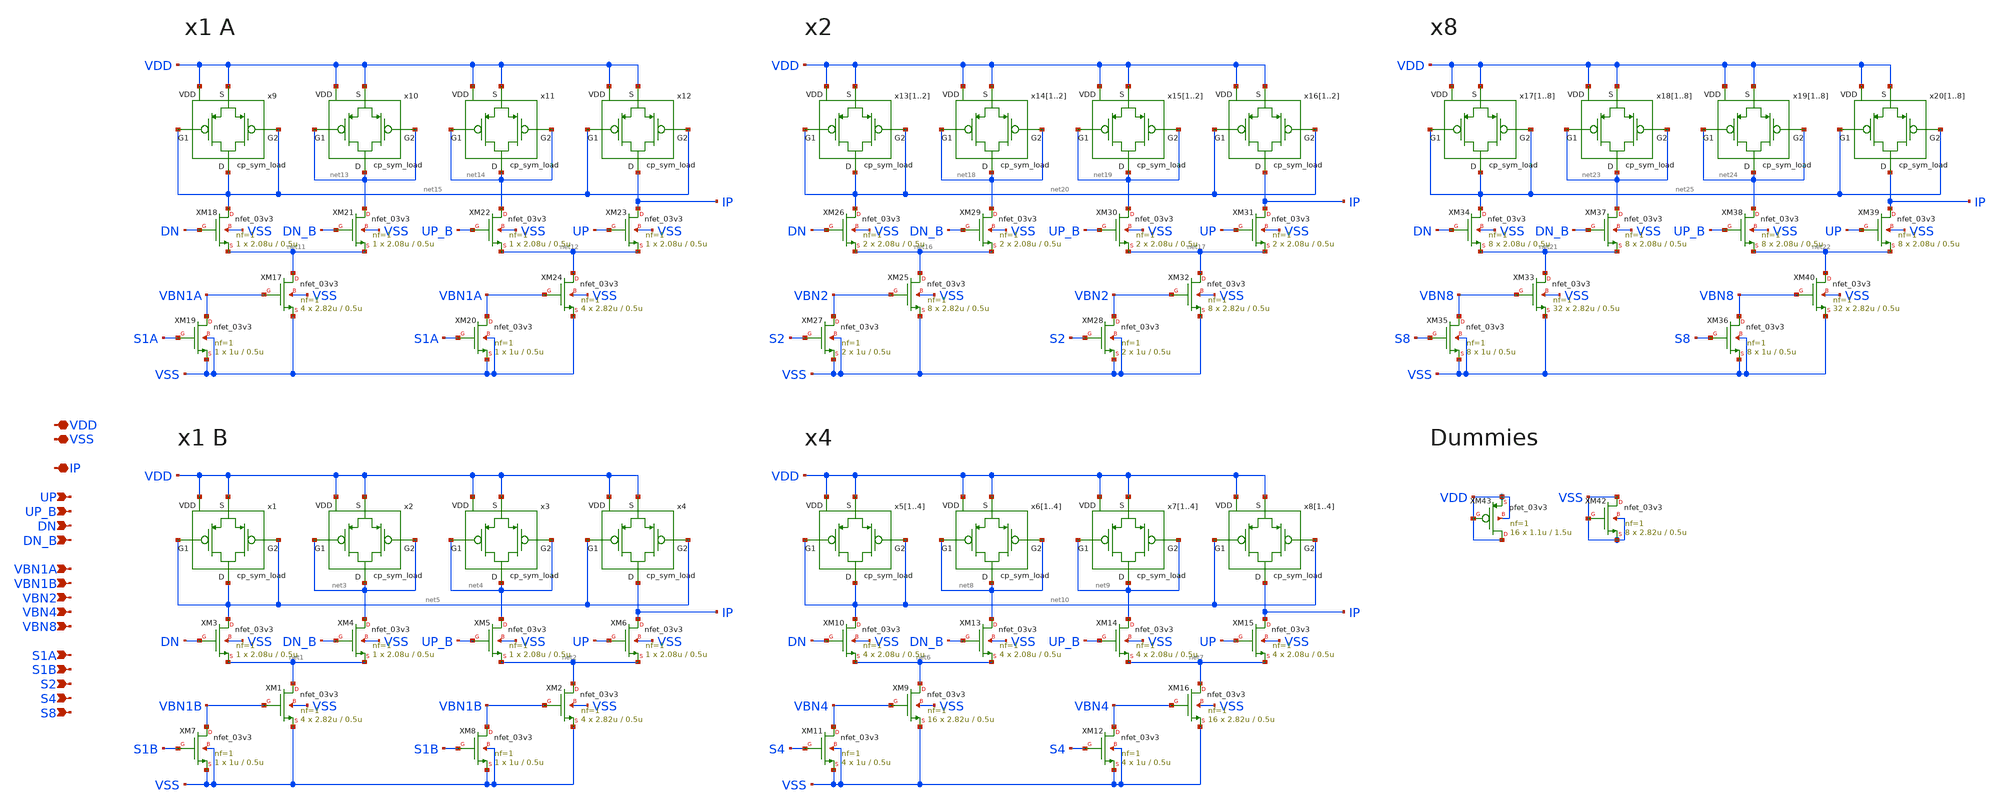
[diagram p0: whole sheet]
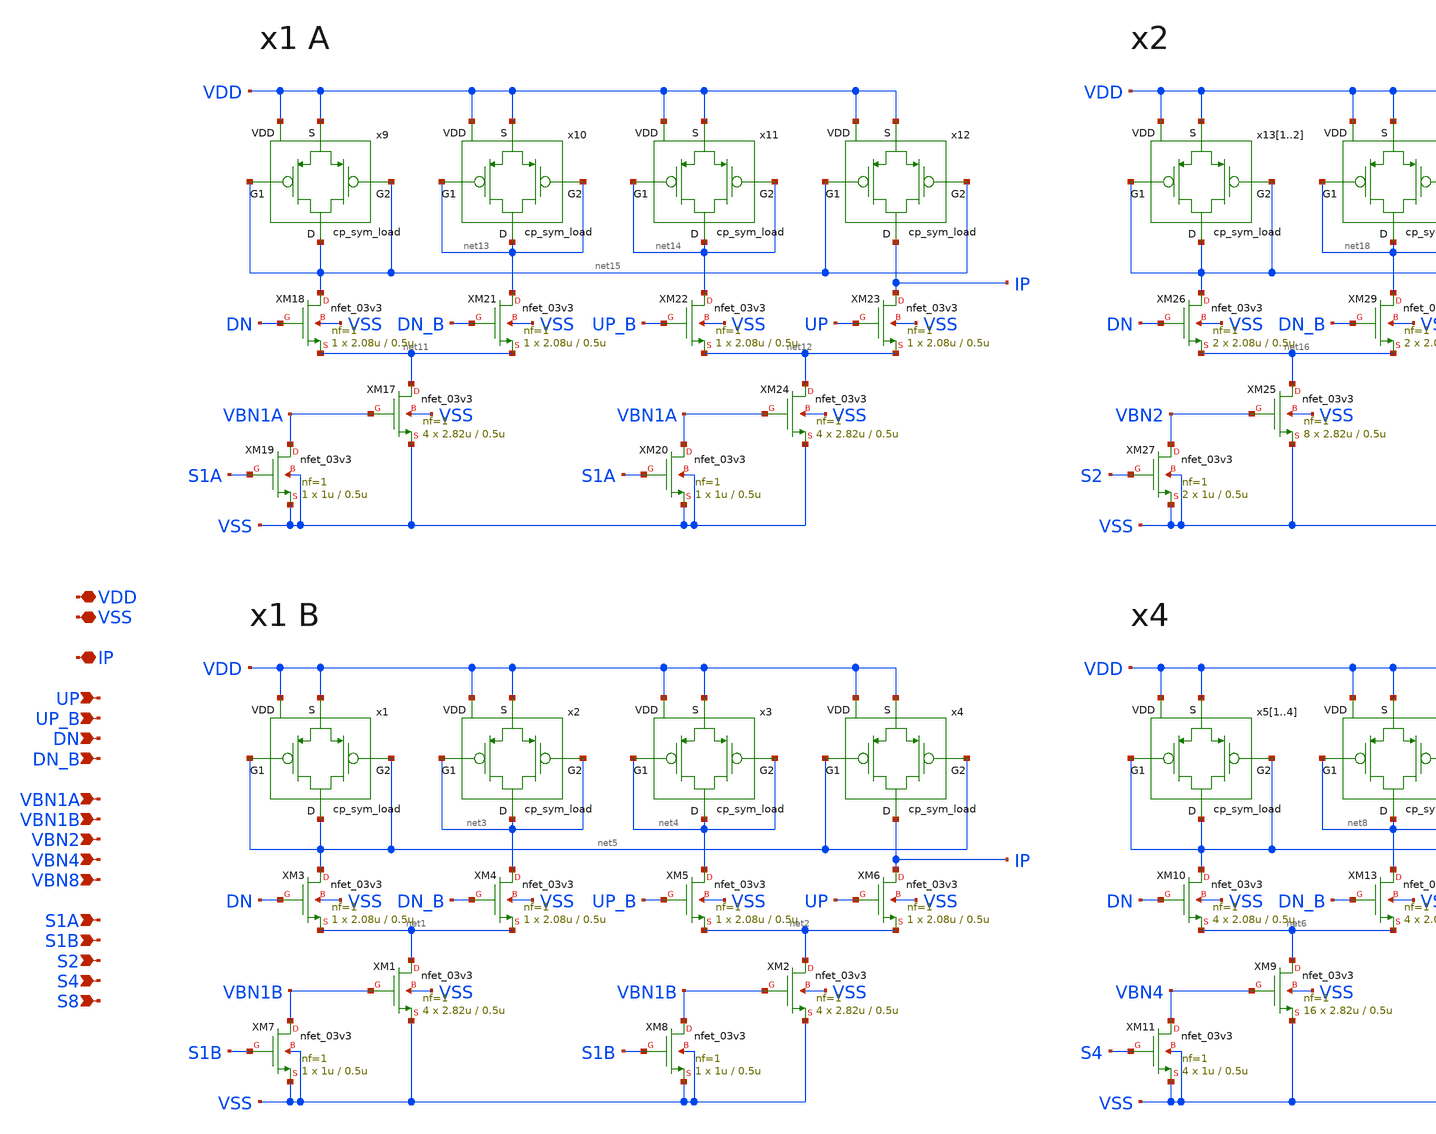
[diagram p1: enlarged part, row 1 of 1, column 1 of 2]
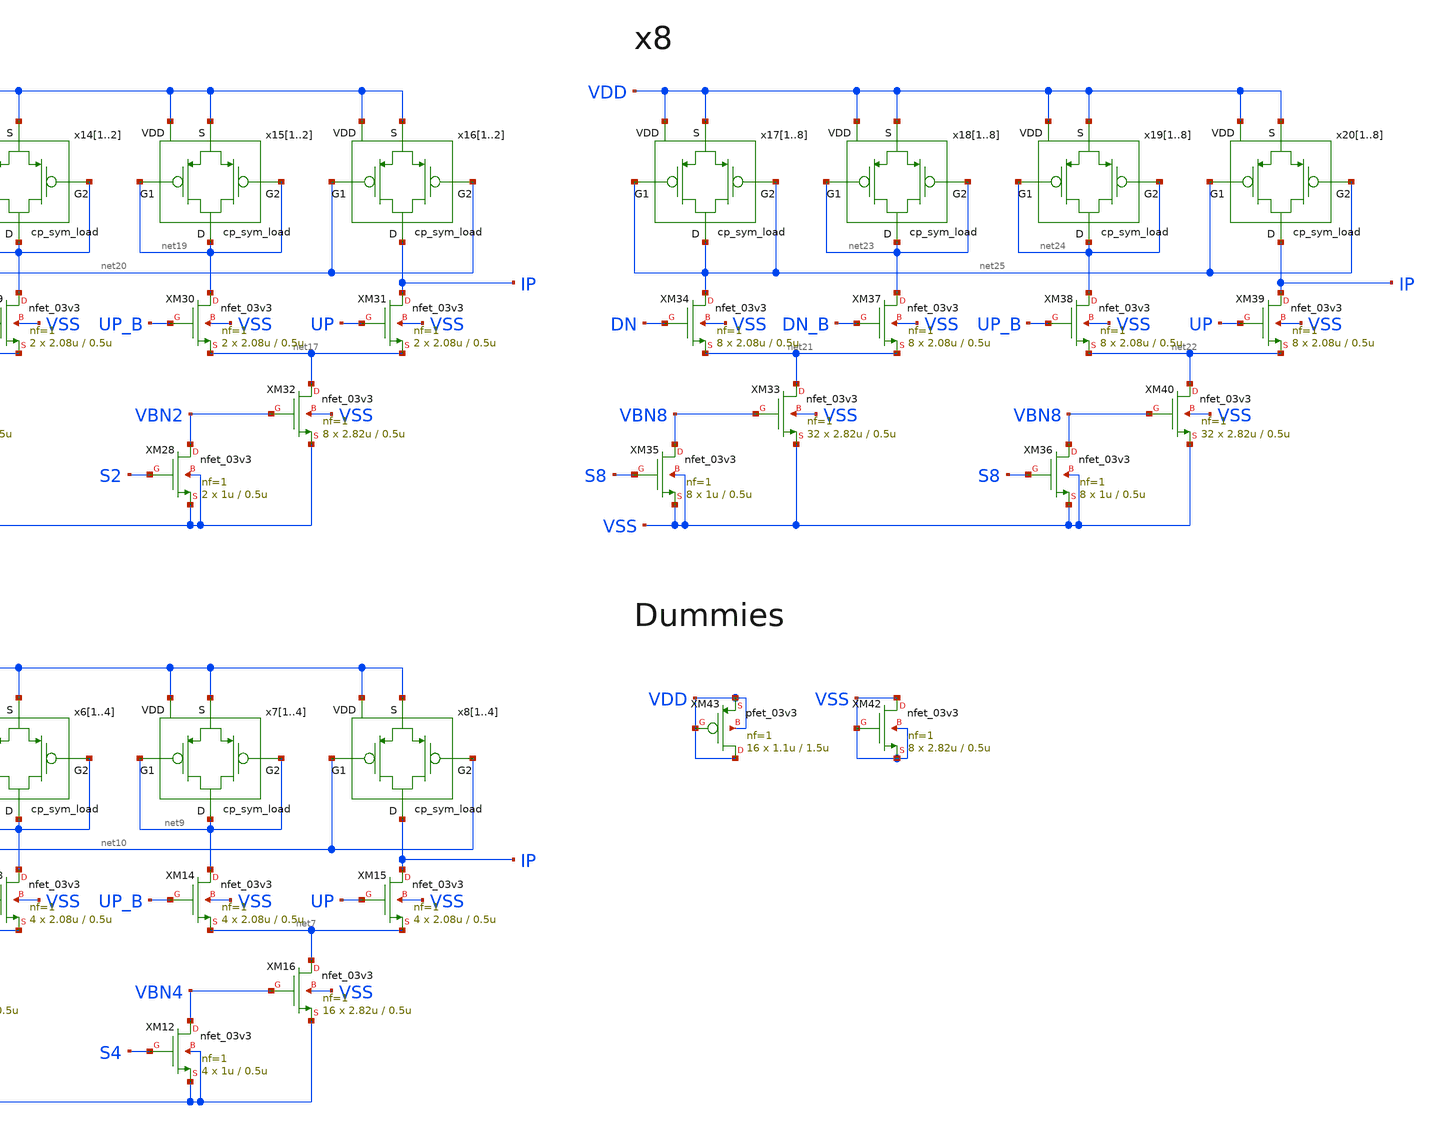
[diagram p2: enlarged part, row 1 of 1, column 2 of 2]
** sch_path: designs/libs/core_analog/charge_pump/charge_pump_top.sch
**.subckt charge_pump_top VDD VSS UP UP_B DN DN_B VBN1A IP S1A VBN1B VBN2 VBN4 VBN8 S1B S2 S4 S8
*.iopin VDD
*.iopin VSS
*.ipin UP
*.ipin UP_B
*.ipin DN
*.ipin DN_B
*.ipin VBN1A
*.iopin IP
*.ipin S1A
*.ipin VBN1B
*.ipin VBN2
*.ipin VBN4
*.ipin VBN8
*.ipin S1B
*.ipin S2
*.ipin S4
*.ipin S8
x1 net5 net5 VDD net5 VDD cp_sym_load
x2 net3 net3 VDD net3 VDD cp_sym_load
x3 net4 net4 VDD net4 VDD cp_sym_load
x4 net5 net5 VDD IP VDD cp_sym_load
XM1 net1 VBN1B VSS VSS nfet_03v3 L=0.5u W=2.82u nf=1 ad='int((nf+1)/2) * W/nf * 0.18u' as='int((nf+2)/2) * W/nf * 0.18u'
+ pd='2*int((nf+1)/2) * (W/nf + 0.18u)' ps='2*int((nf+2)/2) * (W/nf + 0.18u)' nrd='0.18u / W' nrs='0.18u / W'
+ sa=0 sb=0 sd=0 m=4
XM3 net5 DN net1 VSS nfet_03v3 L=0.5u W=2.08u nf=1 ad='int((nf+1)/2) * W/nf * 0.18u' as='int((nf+2)/2) * W/nf * 0.18u'
+ pd='2*int((nf+1)/2) * (W/nf + 0.18u)' ps='2*int((nf+2)/2) * (W/nf + 0.18u)' nrd='0.18u / W' nrs='0.18u / W'
+ sa=0 sb=0 sd=0 m=1
XM7 VBN1B S1B VSS VSS nfet_03v3 L=0.5u W=1u nf=1 ad='int((nf+1)/2) * W/nf * 0.18u' as='int((nf+2)/2) * W/nf * 0.18u'
+ pd='2*int((nf+1)/2) * (W/nf + 0.18u)' ps='2*int((nf+2)/2) * (W/nf + 0.18u)' nrd='0.18u / W' nrs='0.18u / W'
+ sa=0 sb=0 sd=0 m=1
XM8 VBN1B S1B VSS VSS nfet_03v3 L=0.5u W=1u nf=1 ad='int((nf+1)/2) * W/nf * 0.18u' as='int((nf+2)/2) * W/nf * 0.18u'
+ pd='2*int((nf+1)/2) * (W/nf + 0.18u)' ps='2*int((nf+2)/2) * (W/nf + 0.18u)' nrd='0.18u / W' nrs='0.18u / W'
+ sa=0 sb=0 sd=0 m=1
XM4 net3 DN_B net1 VSS nfet_03v3 L=0.5u W=2.08u nf=1 ad='int((nf+1)/2) * W/nf * 0.18u' as='int((nf+2)/2) * W/nf * 0.18u'
+ pd='2*int((nf+1)/2) * (W/nf + 0.18u)' ps='2*int((nf+2)/2) * (W/nf + 0.18u)' nrd='0.18u / W' nrs='0.18u / W'
+ sa=0 sb=0 sd=0 m=1
XM5 net4 UP_B net2 VSS nfet_03v3 L=0.5u W=2.08u nf=1 ad='int((nf+1)/2) * W/nf * 0.18u' as='int((nf+2)/2) * W/nf * 0.18u'
+ pd='2*int((nf+1)/2) * (W/nf + 0.18u)' ps='2*int((nf+2)/2) * (W/nf + 0.18u)' nrd='0.18u / W' nrs='0.18u / W'
+ sa=0 sb=0 sd=0 m=1
XM6 IP UP net2 VSS nfet_03v3 L=0.5u W=2.08u nf=1 ad='int((nf+1)/2) * W/nf * 0.18u' as='int((nf+2)/2) * W/nf * 0.18u'
+ pd='2*int((nf+1)/2) * (W/nf + 0.18u)' ps='2*int((nf+2)/2) * (W/nf + 0.18u)' nrd='0.18u / W' nrs='0.18u / W'
+ sa=0 sb=0 sd=0 m=1
XM2 net2 VBN1B VSS VSS nfet_03v3 L=0.5u W=2.82u nf=1 ad='int((nf+1)/2) * W/nf * 0.18u' as='int((nf+2)/2) * W/nf * 0.18u'
+ pd='2*int((nf+1)/2) * (W/nf + 0.18u)' ps='2*int((nf+2)/2) * (W/nf + 0.18u)' nrd='0.18u / W' nrs='0.18u / W'
+ sa=0 sb=0 sd=0 m=4
x51 net10 net10 VDD net10 VDD cp_sym_load
x52 net10 net10 VDD net10 VDD cp_sym_load
x53 net10 net10 VDD net10 VDD cp_sym_load
x54 net10 net10 VDD net10 VDD cp_sym_load
x61 net8 net8 VDD net8 VDD cp_sym_load
x62 net8 net8 VDD net8 VDD cp_sym_load
x63 net8 net8 VDD net8 VDD cp_sym_load
x64 net8 net8 VDD net8 VDD cp_sym_load
x71 net9 net9 VDD net9 VDD cp_sym_load
x72 net9 net9 VDD net9 VDD cp_sym_load
x73 net9 net9 VDD net9 VDD cp_sym_load
x74 net9 net9 VDD net9 VDD cp_sym_load
x81 net10 net10 VDD IP VDD cp_sym_load
x82 net10 net10 VDD IP VDD cp_sym_load
x83 net10 net10 VDD IP VDD cp_sym_load
x84 net10 net10 VDD IP VDD cp_sym_load
XM9 net6 VBN4 VSS VSS nfet_03v3 L=0.5u W=2.82u nf=1 ad='int((nf+1)/2) * W/nf * 0.18u' as='int((nf+2)/2) * W/nf * 0.18u'
+ pd='2*int((nf+1)/2) * (W/nf + 0.18u)' ps='2*int((nf+2)/2) * (W/nf + 0.18u)' nrd='0.18u / W' nrs='0.18u / W'
+ sa=0 sb=0 sd=0 m=16
XM10 net10 DN net6 VSS nfet_03v3 L=0.5u W=2.08u nf=1 ad='int((nf+1)/2) * W/nf * 0.18u' as='int((nf+2)/2) * W/nf * 0.18u'
+ pd='2*int((nf+1)/2) * (W/nf + 0.18u)' ps='2*int((nf+2)/2) * (W/nf + 0.18u)' nrd='0.18u / W' nrs='0.18u / W'
+ sa=0 sb=0 sd=0 m=4
XM11 VBN4 S4 VSS VSS nfet_03v3 L=0.5u W=1u nf=1 ad='int((nf+1)/2) * W/nf * 0.18u' as='int((nf+2)/2) * W/nf * 0.18u'
+ pd='2*int((nf+1)/2) * (W/nf + 0.18u)' ps='2*int((nf+2)/2) * (W/nf + 0.18u)' nrd='0.18u / W' nrs='0.18u / W'
+ sa=0 sb=0 sd=0 m=4
XM12 VBN4 S4 VSS VSS nfet_03v3 L=0.5u W=1u nf=1 ad='int((nf+1)/2) * W/nf * 0.18u' as='int((nf+2)/2) * W/nf * 0.18u'
+ pd='2*int((nf+1)/2) * (W/nf + 0.18u)' ps='2*int((nf+2)/2) * (W/nf + 0.18u)' nrd='0.18u / W' nrs='0.18u / W'
+ sa=0 sb=0 sd=0 m=4
XM13 net8 DN_B net6 VSS nfet_03v3 L=0.5u W=2.08u nf=1 ad='int((nf+1)/2) * W/nf * 0.18u' as='int((nf+2)/2) * W/nf * 0.18u'
+ pd='2*int((nf+1)/2) * (W/nf + 0.18u)' ps='2*int((nf+2)/2) * (W/nf + 0.18u)' nrd='0.18u / W' nrs='0.18u / W'
+ sa=0 sb=0 sd=0 m=4
XM14 net9 UP_B net7 VSS nfet_03v3 L=0.5u W=2.08u nf=1 ad='int((nf+1)/2) * W/nf * 0.18u' as='int((nf+2)/2) * W/nf * 0.18u'
+ pd='2*int((nf+1)/2) * (W/nf + 0.18u)' ps='2*int((nf+2)/2) * (W/nf + 0.18u)' nrd='0.18u / W' nrs='0.18u / W'
+ sa=0 sb=0 sd=0 m=4
XM15 IP UP net7 VSS nfet_03v3 L=0.5u W=2.08u nf=1 ad='int((nf+1)/2) * W/nf * 0.18u' as='int((nf+2)/2) * W/nf * 0.18u'
+ pd='2*int((nf+1)/2) * (W/nf + 0.18u)' ps='2*int((nf+2)/2) * (W/nf + 0.18u)' nrd='0.18u / W' nrs='0.18u / W'
+ sa=0 sb=0 sd=0 m=4
XM16 net7 VBN4 VSS VSS nfet_03v3 L=0.5u W=2.82u nf=1 ad='int((nf+1)/2) * W/nf * 0.18u' as='int((nf+2)/2) * W/nf * 0.18u'
+ pd='2*int((nf+1)/2) * (W/nf + 0.18u)' ps='2*int((nf+2)/2) * (W/nf + 0.18u)' nrd='0.18u / W' nrs='0.18u / W'
+ sa=0 sb=0 sd=0 m=16
x9 net15 net15 VDD net15 VDD cp_sym_load
x10 net13 net13 VDD net13 VDD cp_sym_load
x11 net14 net14 VDD net14 VDD cp_sym_load
x12 net15 net15 VDD IP VDD cp_sym_load
XM17 net11 VBN1A VSS VSS nfet_03v3 L=0.5u W=2.82u nf=1 ad='int((nf+1)/2) * W/nf * 0.18u' as='int((nf+2)/2) * W/nf * 0.18u'
+ pd='2*int((nf+1)/2) * (W/nf + 0.18u)' ps='2*int((nf+2)/2) * (W/nf + 0.18u)' nrd='0.18u / W' nrs='0.18u / W'
+ sa=0 sb=0 sd=0 m=4
XM18 net15 DN net11 VSS nfet_03v3 L=0.5u W=2.08u nf=1 ad='int((nf+1)/2) * W/nf * 0.18u' as='int((nf+2)/2) * W/nf * 0.18u'
+ pd='2*int((nf+1)/2) * (W/nf + 0.18u)' ps='2*int((nf+2)/2) * (W/nf + 0.18u)' nrd='0.18u / W' nrs='0.18u / W'
+ sa=0 sb=0 sd=0 m=1
XM19 VBN1A S1A VSS VSS nfet_03v3 L=0.5u W=1u nf=1 ad='int((nf+1)/2) * W/nf * 0.18u' as='int((nf+2)/2) * W/nf * 0.18u'
+ pd='2*int((nf+1)/2) * (W/nf + 0.18u)' ps='2*int((nf+2)/2) * (W/nf + 0.18u)' nrd='0.18u / W' nrs='0.18u / W'
+ sa=0 sb=0 sd=0 m=1
XM20 VBN1A S1A VSS VSS nfet_03v3 L=0.5u W=1u nf=1 ad='int((nf+1)/2) * W/nf * 0.18u' as='int((nf+2)/2) * W/nf * 0.18u'
+ pd='2*int((nf+1)/2) * (W/nf + 0.18u)' ps='2*int((nf+2)/2) * (W/nf + 0.18u)' nrd='0.18u / W' nrs='0.18u / W'
+ sa=0 sb=0 sd=0 m=1
XM21 net13 DN_B net11 VSS nfet_03v3 L=0.5u W=2.08u nf=1 ad='int((nf+1)/2) * W/nf * 0.18u' as='int((nf+2)/2) * W/nf * 0.18u'
+ pd='2*int((nf+1)/2) * (W/nf + 0.18u)' ps='2*int((nf+2)/2) * (W/nf + 0.18u)' nrd='0.18u / W' nrs='0.18u / W'
+ sa=0 sb=0 sd=0 m=1
XM22 net14 UP_B net12 VSS nfet_03v3 L=0.5u W=2.08u nf=1 ad='int((nf+1)/2) * W/nf * 0.18u' as='int((nf+2)/2) * W/nf * 0.18u'
+ pd='2*int((nf+1)/2) * (W/nf + 0.18u)' ps='2*int((nf+2)/2) * (W/nf + 0.18u)' nrd='0.18u / W' nrs='0.18u / W'
+ sa=0 sb=0 sd=0 m=1
XM23 IP UP net12 VSS nfet_03v3 L=0.5u W=2.08u nf=1 ad='int((nf+1)/2) * W/nf * 0.18u' as='int((nf+2)/2) * W/nf * 0.18u'
+ pd='2*int((nf+1)/2) * (W/nf + 0.18u)' ps='2*int((nf+2)/2) * (W/nf + 0.18u)' nrd='0.18u / W' nrs='0.18u / W'
+ sa=0 sb=0 sd=0 m=1
XM24 net12 VBN1A VSS VSS nfet_03v3 L=0.5u W=2.82u nf=1 ad='int((nf+1)/2) * W/nf * 0.18u' as='int((nf+2)/2) * W/nf * 0.18u'
+ pd='2*int((nf+1)/2) * (W/nf + 0.18u)' ps='2*int((nf+2)/2) * (W/nf + 0.18u)' nrd='0.18u / W' nrs='0.18u / W'
+ sa=0 sb=0 sd=0 m=4
x131 net20 net20 VDD net20 VDD cp_sym_load
x132 net20 net20 VDD net20 VDD cp_sym_load
x141 net18 net18 VDD net18 VDD cp_sym_load
x142 net18 net18 VDD net18 VDD cp_sym_load
x151 net19 net19 VDD net19 VDD cp_sym_load
x152 net19 net19 VDD net19 VDD cp_sym_load
x161 net20 net20 VDD IP VDD cp_sym_load
x162 net20 net20 VDD IP VDD cp_sym_load
XM25 net16 VBN2 VSS VSS nfet_03v3 L=0.5u W=2.82u nf=1 ad='int((nf+1)/2) * W/nf * 0.18u' as='int((nf+2)/2) * W/nf * 0.18u'
+ pd='2*int((nf+1)/2) * (W/nf + 0.18u)' ps='2*int((nf+2)/2) * (W/nf + 0.18u)' nrd='0.18u / W' nrs='0.18u / W'
+ sa=0 sb=0 sd=0 m=8
XM26 net20 DN net16 VSS nfet_03v3 L=0.5u W=2.08u nf=1 ad='int((nf+1)/2) * W/nf * 0.18u' as='int((nf+2)/2) * W/nf * 0.18u'
+ pd='2*int((nf+1)/2) * (W/nf + 0.18u)' ps='2*int((nf+2)/2) * (W/nf + 0.18u)' nrd='0.18u / W' nrs='0.18u / W'
+ sa=0 sb=0 sd=0 m=2
XM27 VBN2 S2 VSS VSS nfet_03v3 L=0.5u W=1u nf=1 ad='int((nf+1)/2) * W/nf * 0.18u' as='int((nf+2)/2) * W/nf * 0.18u'
+ pd='2*int((nf+1)/2) * (W/nf + 0.18u)' ps='2*int((nf+2)/2) * (W/nf + 0.18u)' nrd='0.18u / W' nrs='0.18u / W'
+ sa=0 sb=0 sd=0 m=2
XM28 VBN2 S2 VSS VSS nfet_03v3 L=0.5u W=1u nf=1 ad='int((nf+1)/2) * W/nf * 0.18u' as='int((nf+2)/2) * W/nf * 0.18u'
+ pd='2*int((nf+1)/2) * (W/nf + 0.18u)' ps='2*int((nf+2)/2) * (W/nf + 0.18u)' nrd='0.18u / W' nrs='0.18u / W'
+ sa=0 sb=0 sd=0 m=2
XM29 net18 DN_B net16 VSS nfet_03v3 L=0.5u W=2.08u nf=1 ad='int((nf+1)/2) * W/nf * 0.18u' as='int((nf+2)/2) * W/nf * 0.18u'
+ pd='2*int((nf+1)/2) * (W/nf + 0.18u)' ps='2*int((nf+2)/2) * (W/nf + 0.18u)' nrd='0.18u / W' nrs='0.18u / W'
+ sa=0 sb=0 sd=0 m=2
XM30 net19 UP_B net17 VSS nfet_03v3 L=0.5u W=2.08u nf=1 ad='int((nf+1)/2) * W/nf * 0.18u' as='int((nf+2)/2) * W/nf * 0.18u'
+ pd='2*int((nf+1)/2) * (W/nf + 0.18u)' ps='2*int((nf+2)/2) * (W/nf + 0.18u)' nrd='0.18u / W' nrs='0.18u / W'
+ sa=0 sb=0 sd=0 m=2
XM31 IP UP net17 VSS nfet_03v3 L=0.5u W=2.08u nf=1 ad='int((nf+1)/2) * W/nf * 0.18u' as='int((nf+2)/2) * W/nf * 0.18u'
+ pd='2*int((nf+1)/2) * (W/nf + 0.18u)' ps='2*int((nf+2)/2) * (W/nf + 0.18u)' nrd='0.18u / W' nrs='0.18u / W'
+ sa=0 sb=0 sd=0 m=2
XM32 net17 VBN2 VSS VSS nfet_03v3 L=0.5u W=2.82u nf=1 ad='int((nf+1)/2) * W/nf * 0.18u' as='int((nf+2)/2) * W/nf * 0.18u'
+ pd='2*int((nf+1)/2) * (W/nf + 0.18u)' ps='2*int((nf+2)/2) * (W/nf + 0.18u)' nrd='0.18u / W' nrs='0.18u / W'
+ sa=0 sb=0 sd=0 m=8
x171 net25 net25 VDD net25 VDD cp_sym_load
x172 net25 net25 VDD net25 VDD cp_sym_load
x173 net25 net25 VDD net25 VDD cp_sym_load
x174 net25 net25 VDD net25 VDD cp_sym_load
x175 net25 net25 VDD net25 VDD cp_sym_load
x176 net25 net25 VDD net25 VDD cp_sym_load
x177 net25 net25 VDD net25 VDD cp_sym_load
x178 net25 net25 VDD net25 VDD cp_sym_load
x181 net23 net23 VDD net23 VDD cp_sym_load
x182 net23 net23 VDD net23 VDD cp_sym_load
x183 net23 net23 VDD net23 VDD cp_sym_load
x184 net23 net23 VDD net23 VDD cp_sym_load
x185 net23 net23 VDD net23 VDD cp_sym_load
x186 net23 net23 VDD net23 VDD cp_sym_load
x187 net23 net23 VDD net23 VDD cp_sym_load
x188 net23 net23 VDD net23 VDD cp_sym_load
x191 net24 net24 VDD net24 VDD cp_sym_load
x192 net24 net24 VDD net24 VDD cp_sym_load
x193 net24 net24 VDD net24 VDD cp_sym_load
x194 net24 net24 VDD net24 VDD cp_sym_load
x195 net24 net24 VDD net24 VDD cp_sym_load
x196 net24 net24 VDD net24 VDD cp_sym_load
x197 net24 net24 VDD net24 VDD cp_sym_load
x198 net24 net24 VDD net24 VDD cp_sym_load
x201 net25 net25 VDD IP VDD cp_sym_load
x202 net25 net25 VDD IP VDD cp_sym_load
x203 net25 net25 VDD IP VDD cp_sym_load
x204 net25 net25 VDD IP VDD cp_sym_load
x205 net25 net25 VDD IP VDD cp_sym_load
x206 net25 net25 VDD IP VDD cp_sym_load
x207 net25 net25 VDD IP VDD cp_sym_load
x208 net25 net25 VDD IP VDD cp_sym_load
XM33 net21 VBN8 VSS VSS nfet_03v3 L=0.5u W=2.82u nf=1 ad='int((nf+1)/2) * W/nf * 0.18u' as='int((nf+2)/2) * W/nf * 0.18u'
+ pd='2*int((nf+1)/2) * (W/nf + 0.18u)' ps='2*int((nf+2)/2) * (W/nf + 0.18u)' nrd='0.18u / W' nrs='0.18u / W'
+ sa=0 sb=0 sd=0 m=32
XM34 net25 DN net21 VSS nfet_03v3 L=0.5u W=2.08u nf=1 ad='int((nf+1)/2) * W/nf * 0.18u' as='int((nf+2)/2) * W/nf * 0.18u'
+ pd='2*int((nf+1)/2) * (W/nf + 0.18u)' ps='2*int((nf+2)/2) * (W/nf + 0.18u)' nrd='0.18u / W' nrs='0.18u / W'
+ sa=0 sb=0 sd=0 m=8
XM35 VBN8 S8 VSS VSS nfet_03v3 L=0.5u W=1u nf=1 ad='int((nf+1)/2) * W/nf * 0.18u' as='int((nf+2)/2) * W/nf * 0.18u'
+ pd='2*int((nf+1)/2) * (W/nf + 0.18u)' ps='2*int((nf+2)/2) * (W/nf + 0.18u)' nrd='0.18u / W' nrs='0.18u / W'
+ sa=0 sb=0 sd=0 m=8
XM36 VBN8 S8 VSS VSS nfet_03v3 L=0.5u W=1u nf=1 ad='int((nf+1)/2) * W/nf * 0.18u' as='int((nf+2)/2) * W/nf * 0.18u'
+ pd='2*int((nf+1)/2) * (W/nf + 0.18u)' ps='2*int((nf+2)/2) * (W/nf + 0.18u)' nrd='0.18u / W' nrs='0.18u / W'
+ sa=0 sb=0 sd=0 m=8
XM37 net23 DN_B net21 VSS nfet_03v3 L=0.5u W=2.08u nf=1 ad='int((nf+1)/2) * W/nf * 0.18u' as='int((nf+2)/2) * W/nf * 0.18u'
+ pd='2*int((nf+1)/2) * (W/nf + 0.18u)' ps='2*int((nf+2)/2) * (W/nf + 0.18u)' nrd='0.18u / W' nrs='0.18u / W'
+ sa=0 sb=0 sd=0 m=8
XM38 net24 UP_B net22 VSS nfet_03v3 L=0.5u W=2.08u nf=1 ad='int((nf+1)/2) * W/nf * 0.18u' as='int((nf+2)/2) * W/nf * 0.18u'
+ pd='2*int((nf+1)/2) * (W/nf + 0.18u)' ps='2*int((nf+2)/2) * (W/nf + 0.18u)' nrd='0.18u / W' nrs='0.18u / W'
+ sa=0 sb=0 sd=0 m=8
XM39 IP UP net22 VSS nfet_03v3 L=0.5u W=2.08u nf=1 ad='int((nf+1)/2) * W/nf * 0.18u' as='int((nf+2)/2) * W/nf * 0.18u'
+ pd='2*int((nf+1)/2) * (W/nf + 0.18u)' ps='2*int((nf+2)/2) * (W/nf + 0.18u)' nrd='0.18u / W' nrs='0.18u / W'
+ sa=0 sb=0 sd=0 m=8
XM40 net22 VBN8 VSS VSS nfet_03v3 L=0.5u W=2.82u nf=1 ad='int((nf+1)/2) * W/nf * 0.18u' as='int((nf+2)/2) * W/nf * 0.18u'
+ pd='2*int((nf+1)/2) * (W/nf + 0.18u)' ps='2*int((nf+2)/2) * (W/nf + 0.18u)' nrd='0.18u / W' nrs='0.18u / W'
+ sa=0 sb=0 sd=0 m=32
XM42 VSS VSS VSS VSS nfet_03v3 L=0.5u W=2.82u nf=1 ad='int((nf+1)/2) * W/nf * 0.18u' as='int((nf+2)/2) * W/nf * 0.18u'
+ pd='2*int((nf+1)/2) * (W/nf + 0.18u)' ps='2*int((nf+2)/2) * (W/nf + 0.18u)' nrd='0.18u / W' nrs='0.18u / W'
+ sa=0 sb=0 sd=0 m=8
XM43 VDD VDD VDD VDD pfet_03v3 L=1.5u W=1.1u nf=1 ad='int((nf+1)/2) * W/nf * 0.18u' as='int((nf+2)/2) * W/nf * 0.18u'
+ pd='2*int((nf+1)/2) * (W/nf + 0.18u)' ps='2*int((nf+2)/2) * (W/nf + 0.18u)' nrd='0.18u / W' nrs='0.18u / W'
+ sa=0 sb=0 sd=0 m=16
**.ends

* expanding   symbol:  libs/core_analog/cp_sym_load/cp_sym_load.sym # of pins=5
** sym_path: designs/libs/core_analog/cp_sym_load/cp_sym_load.sym
** sch_path: designs/libs/core_analog/cp_sym_load/cp_sym_load.sch
.subckt cp_sym_load G1 G2 S D VDD
*.ipin G1
*.ipin G2
*.iopin S
*.iopin D
*.iopin VDD
XM1 D G1 S VDD pfet_03v3 L=1.5u W=1.1u nf=1 ad='int((nf+1)/2) * W/nf * 0.18u' as='int((nf+2)/2) * W/nf * 0.18u'
+ pd='2*int((nf+1)/2) * (W/nf + 0.18u)' ps='2*int((nf+2)/2) * (W/nf + 0.18u)' nrd='0.18u / W' nrs='0.18u / W'
+ sa=0 sb=0 sd=0 m=1
XM2 D G2 S VDD pfet_03v3 L=1.5u W=1.1u nf=1 ad='int((nf+1)/2) * W/nf * 0.18u' as='int((nf+2)/2) * W/nf * 0.18u'
+ pd='2*int((nf+1)/2) * (W/nf + 0.18u)' ps='2*int((nf+2)/2) * (W/nf + 0.18u)' nrd='0.18u / W' nrs='0.18u / W'
+ sa=0 sb=0 sd=0 m=1
.ends

.end
